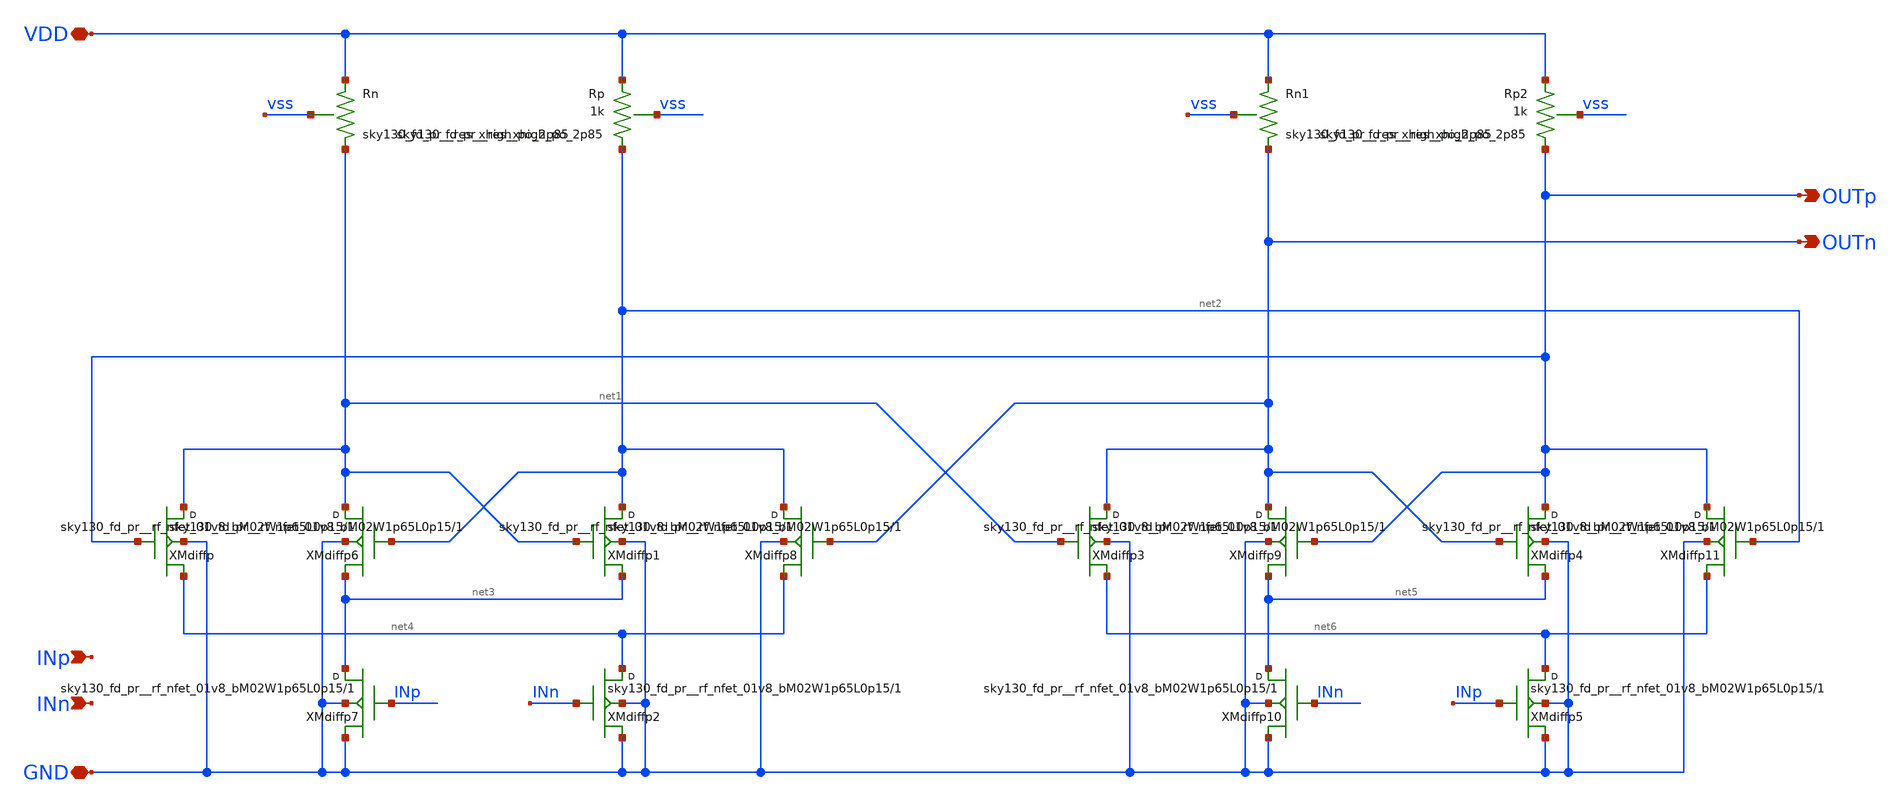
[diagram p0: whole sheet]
** sch_path: design/divider_cml/divider_cml.sch
**.subckt divider_cml INn OUTp VDD GND OUTn INp
*.ipin INn
*.opin OUTp
*.iopin VDD
*.iopin GND
*.opin OUTn
*.ipin INp
XXMdiffp net1 OUTp net4 GND sky130_fd_pr__rf_nfet_01v8_bM02W1p65L0p15 m=1
XXMdiffp1 net2 net1 net3 GND sky130_fd_pr__rf_nfet_01v8_bM02W1p65L0p15 m=1
XXMdiffp2 net4 INn GND GND sky130_fd_pr__rf_nfet_01v8_bM02W1p65L0p15 m=1
XXMdiffp3 OUTn net1 net6 GND sky130_fd_pr__rf_nfet_01v8_bM02W1p65L0p15 m=1
XXMdiffp4 OUTp OUTn net5 GND sky130_fd_pr__rf_nfet_01v8_bM02W1p65L0p15 m=1
XXMdiffp5 net6 INp GND GND sky130_fd_pr__rf_nfet_01v8_bM02W1p65L0p15 m=1
XXMdiffp6 net1 net2 net3 GND sky130_fd_pr__rf_nfet_01v8_bM02W1p65L0p15 m=1
XXMdiffp7 net3 INp GND GND sky130_fd_pr__rf_nfet_01v8_bM02W1p65L0p15 m=1
XXMdiffp8 net2 OUTn net4 GND sky130_fd_pr__rf_nfet_01v8_bM02W1p65L0p15 m=1
XXMdiffp9 OUTn OUTp net5 GND sky130_fd_pr__rf_nfet_01v8_bM02W1p65L0p15 m=1
XXMdiffp10 net5 INn GND GND sky130_fd_pr__rf_nfet_01v8_bM02W1p65L0p15 m=1
XXMdiffp11 OUTp net2 net6 GND sky130_fd_pr__rf_nfet_01v8_bM02W1p65L0p15 m=1
XRn VDD net1 vss sky130_fd_pr__res_xhigh_po_2p85 m=1
XRp VDD net2 vss sky130_fd_pr__res_xhigh_po_2p85 m=1
XRn1 VDD OUTn vss sky130_fd_pr__res_xhigh_po_2p85 m=1
XRp2 VDD OUTp vss sky130_fd_pr__res_xhigh_po_2p85 m=1
**.ends
.end
